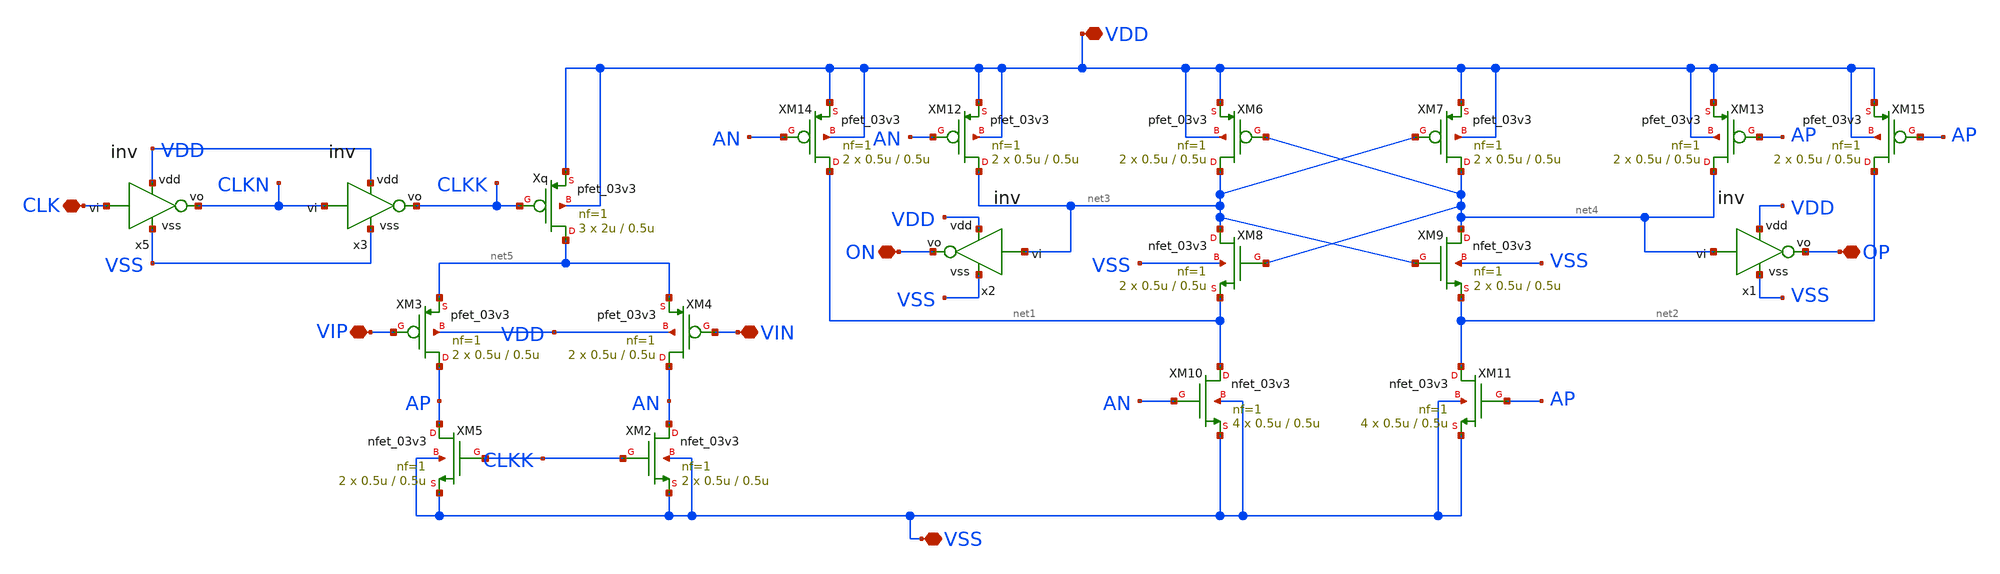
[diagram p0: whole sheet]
** sch_path: designs/sar_adc/comparator/StrongARM/strongARM.sch
**.subckt strongARM VSS VDD VIN VIP OP CLK ON
*.iopin VSS
*.iopin VDD
*.iopin VIN
*.iopin VIP
*.iopin OP
*.iopin CLK
*.iopin ON
Xq net5 CLKK VDD VDD pfet_03v3 L=0.5u W=2u nf=1 ad='int((nf+1)/2) * W/nf * 0.18u' as='int((nf+2)/2) * W/nf * 0.18u'
+ pd='2*int((nf+1)/2) * (W/nf + 0.18u)' ps='2*int((nf+2)/2) * (W/nf + 0.18u)' nrd='0.18u / W' nrs='0.18u / W'
+ sa=0 sb=0 sd=0 m=3
XM2 AN CLKK VSS VSS nfet_03v3 L=0.5u W=0.5u nf=1 ad='int((nf+1)/2) * W/nf * 0.18u' as='int((nf+2)/2) * W/nf * 0.18u'
+ pd='2*int((nf+1)/2) * (W/nf + 0.18u)' ps='2*int((nf+2)/2) * (W/nf + 0.18u)' nrd='0.18u / W' nrs='0.18u / W'
+ sa=0 sb=0 sd=0 m=2
XM3 AP VIP net5 VDD pfet_03v3 L=0.5u W=0.5u nf=1 ad='int((nf+1)/2) * W/nf * 0.18u' as='int((nf+2)/2) * W/nf * 0.18u'
+ pd='2*int((nf+1)/2) * (W/nf + 0.18u)' ps='2*int((nf+2)/2) * (W/nf + 0.18u)' nrd='0.18u / W' nrs='0.18u / W'
+ sa=0 sb=0 sd=0 m=2
XM4 AN VIN net5 VDD pfet_03v3 L=0.5u W=0.5u nf=1 ad='int((nf+1)/2) * W/nf * 0.18u' as='int((nf+2)/2) * W/nf * 0.18u'
+ pd='2*int((nf+1)/2) * (W/nf + 0.18u)' ps='2*int((nf+2)/2) * (W/nf + 0.18u)' nrd='0.18u / W' nrs='0.18u / W'
+ sa=0 sb=0 sd=0 m=2
XM5 AP CLKK VSS VSS nfet_03v3 L=0.5u W=0.5u nf=1 ad='int((nf+1)/2) * W/nf * 0.18u' as='int((nf+2)/2) * W/nf * 0.18u'
+ pd='2*int((nf+1)/2) * (W/nf + 0.18u)' ps='2*int((nf+2)/2) * (W/nf + 0.18u)' nrd='0.18u / W' nrs='0.18u / W'
+ sa=0 sb=0 sd=0 m=2
XM6 net3 net4 VDD VDD pfet_03v3 L=0.5u W=0.5u nf=1 ad='int((nf+1)/2) * W/nf * 0.18u' as='int((nf+2)/2) * W/nf * 0.18u'
+ pd='2*int((nf+1)/2) * (W/nf + 0.18u)' ps='2*int((nf+2)/2) * (W/nf + 0.18u)' nrd='0.18u / W' nrs='0.18u / W'
+ sa=0 sb=0 sd=0 m=2
XM7 net4 net3 VDD VDD pfet_03v3 L=0.5u W=0.5u nf=1 ad='int((nf+1)/2) * W/nf * 0.18u' as='int((nf+2)/2) * W/nf * 0.18u'
+ pd='2*int((nf+1)/2) * (W/nf + 0.18u)' ps='2*int((nf+2)/2) * (W/nf + 0.18u)' nrd='0.18u / W' nrs='0.18u / W'
+ sa=0 sb=0 sd=0 m=2
XM8 net3 net4 net1 VSS nfet_03v3 L=0.5u W=0.5u nf=1 ad='int((nf+1)/2) * W/nf * 0.18u' as='int((nf+2)/2) * W/nf * 0.18u'
+ pd='2*int((nf+1)/2) * (W/nf + 0.18u)' ps='2*int((nf+2)/2) * (W/nf + 0.18u)' nrd='0.18u / W' nrs='0.18u / W'
+ sa=0 sb=0 sd=0 m=2
XM9 net4 net3 net2 VSS nfet_03v3 L=0.5u W=0.5u nf=1 ad='int((nf+1)/2) * W/nf * 0.18u' as='int((nf+2)/2) * W/nf * 0.18u'
+ pd='2*int((nf+1)/2) * (W/nf + 0.18u)' ps='2*int((nf+2)/2) * (W/nf + 0.18u)' nrd='0.18u / W' nrs='0.18u / W'
+ sa=0 sb=0 sd=0 m=2
XM10 net1 AN VSS VSS nfet_03v3 L=0.5u W=0.5u nf=1 ad='int((nf+1)/2) * W/nf * 0.18u' as='int((nf+2)/2) * W/nf * 0.18u'
+ pd='2*int((nf+1)/2) * (W/nf + 0.18u)' ps='2*int((nf+2)/2) * (W/nf + 0.18u)' nrd='0.18u / W' nrs='0.18u / W'
+ sa=0 sb=0 sd=0 m=4
XM11 net2 AP VSS VSS nfet_03v3 L=0.5u W=0.5u nf=1 ad='int((nf+1)/2) * W/nf * 0.18u' as='int((nf+2)/2) * W/nf * 0.18u'
+ pd='2*int((nf+1)/2) * (W/nf + 0.18u)' ps='2*int((nf+2)/2) * (W/nf + 0.18u)' nrd='0.18u / W' nrs='0.18u / W'
+ sa=0 sb=0 sd=0 m=4
XM12 net3 AN VDD VDD pfet_03v3 L=0.5u W=0.5u nf=1 ad='int((nf+1)/2) * W/nf * 0.18u' as='int((nf+2)/2) * W/nf * 0.18u'
+ pd='2*int((nf+1)/2) * (W/nf + 0.18u)' ps='2*int((nf+2)/2) * (W/nf + 0.18u)' nrd='0.18u / W' nrs='0.18u / W'
+ sa=0 sb=0 sd=0 m=2
XM13 net4 AP VDD VDD pfet_03v3 L=0.5u W=0.5u nf=1 ad='int((nf+1)/2) * W/nf * 0.18u' as='int((nf+2)/2) * W/nf * 0.18u'
+ pd='2*int((nf+1)/2) * (W/nf + 0.18u)' ps='2*int((nf+2)/2) * (W/nf + 0.18u)' nrd='0.18u / W' nrs='0.18u / W'
+ sa=0 sb=0 sd=0 m=2
XM14 net1 AN VDD VDD pfet_03v3 L=0.5u W=0.5u nf=1 ad='int((nf+1)/2) * W/nf * 0.18u' as='int((nf+2)/2) * W/nf * 0.18u'
+ pd='2*int((nf+1)/2) * (W/nf + 0.18u)' ps='2*int((nf+2)/2) * (W/nf + 0.18u)' nrd='0.18u / W' nrs='0.18u / W'
+ sa=0 sb=0 sd=0 m=2
XM15 net2 AP VDD VDD pfet_03v3 L=0.5u W=0.5u nf=1 ad='int((nf+1)/2) * W/nf * 0.18u' as='int((nf+2)/2) * W/nf * 0.18u'
+ pd='2*int((nf+1)/2) * (W/nf + 0.18u)' ps='2*int((nf+2)/2) * (W/nf + 0.18u)' nrd='0.18u / W' nrs='0.18u / W'
+ sa=0 sb=0 sd=0 m=2
x1 VDD net4 OP VSS inv
x2 VDD net3 ON VSS inv
x5 VDD CLK CLKN VSS inv
x3 VDD CLKN CLKK VSS inv
**.ends
.end
